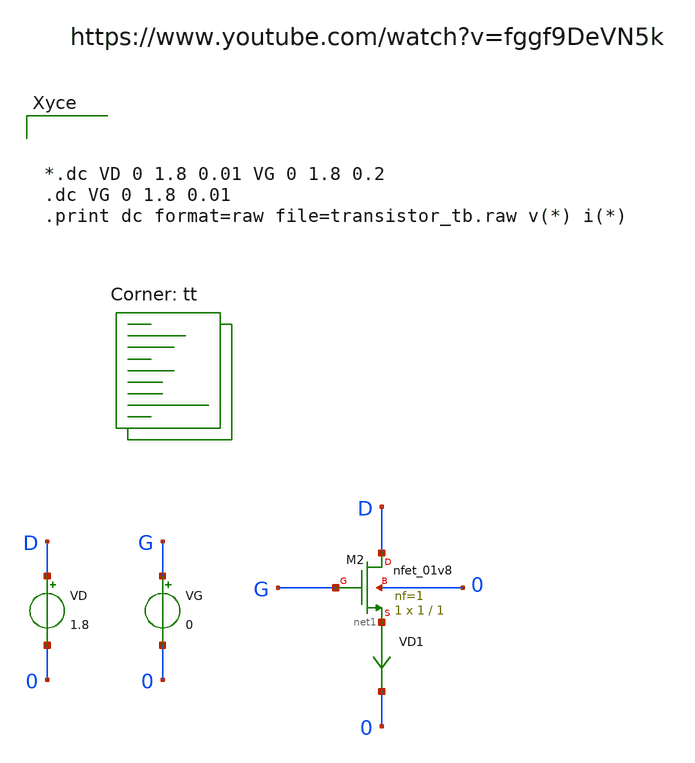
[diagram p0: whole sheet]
** sch_path: design/xschem/transistors_tb.sch
**.subckt transistors_tb
VD D 0 1.8
VD1 net1 0 0
.save i(vd1)
VG G 0 0
XM2 D G net1 0 sky130_fd_pr__nfet_01v8 L=1 W=1 nf=1 ad='int((nf+1)/2) * W/nf * 0.29' as='int((nf+2)/2) * W/nf * 0.29'
+ pd='2*int((nf+1)/2) * (W/nf + 0.29)' ps='2*int((nf+2)/2) * (W/nf + 0.29)' nrd='0.29 / W' nrs='0.29 / W'
+ sa=0 sb=0 sd=0 mult=1 m=1
**** begin user architecture code



*.dc VD 0 1.8 0.01 VG 0 1.8 0.2
.dc VG 0 1.8 0.01
.print dc format=raw file=transistor_tb.raw v(*) i(*)

.lib $::SKYWATER_MODELS/sky130.lib.spice tt
**** end user architecture code
**.ends
.end
